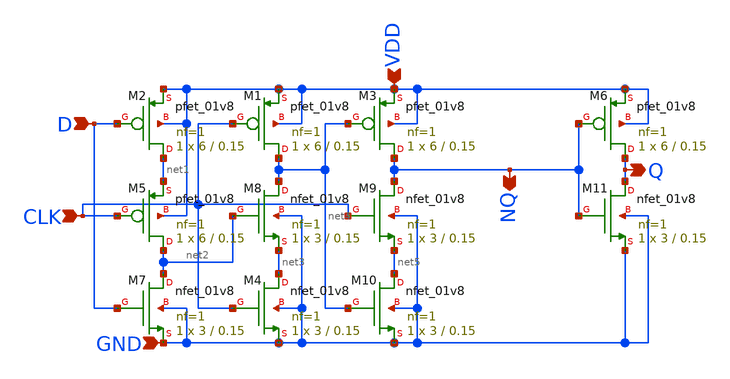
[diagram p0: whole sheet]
** sch_path: sch/DFLIPFLOP.sch
**.subckt DFLIPFLOP CLK D VDD GND Q NQ
*.ipin CLK
*.ipin D
*.ipin VDD
*.ipin GND
*.opin Q
*.opin NQ
XM2 net1 D VDD VDD sky130_fd_pr__pfet_01v8 L=0.15 W=6 nf=1 ad='int((1 + 1)/2) * 6 / 1 * 0.29' as='int((1 + 2)/2) * 6 / 1 * 0.29'
+ pd='2*int((1 + 1)/2) * (6 / 1 + 0.29)' ps='2*int((1 + 2)/2) * (6 / 1 + 0.29)' nrd='0.29 / 6 ' nrs='0.29 / 6 '
+ sa=0 sb=0 sd=0 mult=1 m=1
XM7 net2 D GND GND sky130_fd_pr__nfet_01v8 L=0.15 W=3 nf=1 ad='int((1 + 1)/2) * 3 / 1 * 0.29' as='int((1 + 2)/2) * 3 / 1 * 0.29'
+ pd='2*int((1 + 1)/2) * (3 / 1 + 0.29)' ps='2*int((1 + 2)/2) * (3 / 1 + 0.29)' nrd='0.29 / 3 ' nrs='0.29 / 3 '
+ sa=0 sb=0 sd=0 mult=1 m=1
XM1 net4 CLK VDD VDD sky130_fd_pr__pfet_01v8 L=0.15 W=6 nf=1 ad='int((1 + 1)/2) * 6 / 1 * 0.29' as='int((1 + 2)/2) * 6 / 1 * 0.29'
+ pd='2*int((1 + 1)/2) * (6 / 1 + 0.29)' ps='2*int((1 + 2)/2) * (6 / 1 + 0.29)' nrd='0.29 / 6 ' nrs='0.29 / 6 '
+ sa=0 sb=0 sd=0 mult=1 m=1
XM3 NQ net4 VDD VDD sky130_fd_pr__pfet_01v8 L=0.15 W=6 nf=1 ad='int((1 + 1)/2) * 6 / 1 * 0.29' as='int((1 + 2)/2) * 6 / 1 * 0.29'
+ pd='2*int((1 + 1)/2) * (6 / 1 + 0.29)' ps='2*int((1 + 2)/2) * (6 / 1 + 0.29)' nrd='0.29 / 6 ' nrs='0.29 / 6 '
+ sa=0 sb=0 sd=0 mult=1 m=1
XM5 net2 CLK net1 VDD sky130_fd_pr__pfet_01v8 L=0.15 W=6 nf=1 ad='int((1 + 1)/2) * 6 / 1 * 0.29' as='int((1 + 2)/2) * 6 / 1 * 0.29'
+ pd='2*int((1 + 1)/2) * (6 / 1 + 0.29)' ps='2*int((1 + 2)/2) * (6 / 1 + 0.29)' nrd='0.29 / 6 ' nrs='0.29 / 6 '
+ sa=0 sb=0 sd=0 mult=1 m=1
XM6 Q NQ VDD VDD sky130_fd_pr__pfet_01v8 L=0.15 W=6 nf=1 ad='int((1 + 1)/2) * 6 / 1 * 0.29' as='int((1 + 2)/2) * 6 / 1 * 0.29'
+ pd='2*int((1 + 1)/2) * (6 / 1 + 0.29)' ps='2*int((1 + 2)/2) * (6 / 1 + 0.29)' nrd='0.29 / 6 ' nrs='0.29 / 6 '
+ sa=0 sb=0 sd=0 mult=1 m=1
XM4 net3 CLK GND GND sky130_fd_pr__nfet_01v8 L=0.15 W=3 nf=1 ad='int((1 + 1)/2) * 3 / 1 * 0.29' as='int((1 + 2)/2) * 3 / 1 * 0.29'
+ pd='2*int((1 + 1)/2) * (3 / 1 + 0.29)' ps='2*int((1 + 2)/2) * (3 / 1 + 0.29)' nrd='0.29 / 3 ' nrs='0.29 / 3 '
+ sa=0 sb=0 sd=0 mult=1 m=1
XM8 net4 net2 net3 GND sky130_fd_pr__nfet_01v8 L=0.15 W=3 nf=1 ad='int((1 + 1)/2) * 3 / 1 * 0.29' as='int((1 + 2)/2) * 3 / 1 * 0.29'
+ pd='2*int((1 + 1)/2) * (3 / 1 + 0.29)' ps='2*int((1 + 2)/2) * (3 / 1 + 0.29)' nrd='0.29 / 3 ' nrs='0.29 / 3 '
+ sa=0 sb=0 sd=0 mult=1 m=1
XM9 NQ CLK net5 GND sky130_fd_pr__nfet_01v8 L=0.15 W=3 nf=1 ad='int((1 + 1)/2) * 3 / 1 * 0.29' as='int((1 + 2)/2) * 3 / 1 * 0.29'
+ pd='2*int((1 + 1)/2) * (3 / 1 + 0.29)' ps='2*int((1 + 2)/2) * (3 / 1 + 0.29)' nrd='0.29 / 3 ' nrs='0.29 / 3 '
+ sa=0 sb=0 sd=0 mult=1 m=1
XM10 net5 net4 GND GND sky130_fd_pr__nfet_01v8 L=0.15 W=3 nf=1 ad='int((1 + 1)/2) * 3 / 1 * 0.29' as='int((1 + 2)/2) * 3 / 1 * 0.29'
+ pd='2*int((1 + 1)/2) * (3 / 1 + 0.29)' ps='2*int((1 + 2)/2) * (3 / 1 + 0.29)' nrd='0.29 / 3 ' nrs='0.29 / 3 '
+ sa=0 sb=0 sd=0 mult=1 m=1
XM11 Q NQ GND GND sky130_fd_pr__nfet_01v8 L=0.15 W=3 nf=1 ad='int((1 + 1)/2) * 3 / 1 * 0.29' as='int((1 + 2)/2) * 3 / 1 * 0.29'
+ pd='2*int((1 + 1)/2) * (3 / 1 + 0.29)' ps='2*int((1 + 2)/2) * (3 / 1 + 0.29)' nrd='0.29 / 3 ' nrs='0.29 / 3 '
+ sa=0 sb=0 sd=0 mult=1 m=1
**.ends
.end
